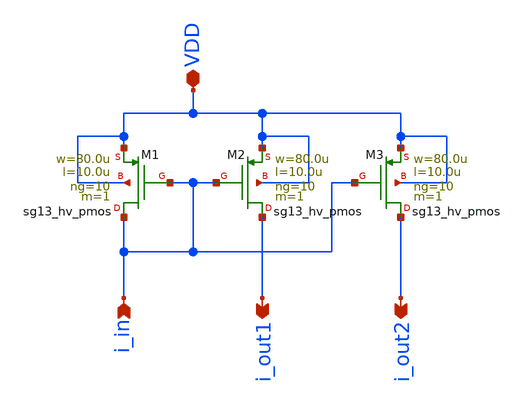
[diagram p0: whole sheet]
** sch_path: macros/heichips26_vcr/macros/switched_capacitor/schematic/xschem/pmos_current_mirror2.sch
**.subckt pmos_current_mirror2 i_in i_out1 VDD i_out2
*.ipin i_in
*.opin i_out1
*.iopin VDD
*.opin i_out2
XM2 i_out1 i_in VDD VDD sg13_hv_pmos w=80.0u l=10.0u ng=10 m=1 mm_ok=1
XM1 i_in i_in VDD VDD sg13_hv_pmos w=80.0u l=10.0u ng=10 m=1 mm_ok=1
XM3 i_out2 i_in VDD VDD sg13_hv_pmos w=80.0u l=10.0u ng=10 m=1 mm_ok=1
**.ends
.end
